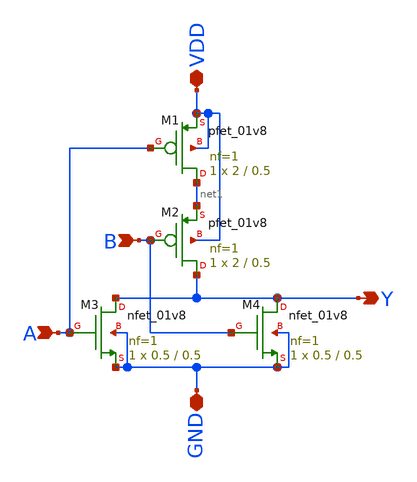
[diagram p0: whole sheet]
** sch_path: FinalProj/NOR.sch
**.subckt NOR B A GND VDD Y
*.ipin B
*.ipin A
*.iopin GND
*.iopin VDD
*.opin Y
XM1 net1 A VDD VDD sky130_fd_pr__pfet_01v8 L=0.5 W=2 nf=1 ad='int((nf+1)/2) * W/nf * 0.29' as='int((nf+2)/2) * W/nf * 0.29'
+ pd='2*int((nf+1)/2) * (W/nf + 0.29)' ps='2*int((nf+2)/2) * (W/nf + 0.29)' nrd='0.29 / W' nrs='0.29 / W'
+ sa=0 sb=0 sd=0 mult=1 m=1
XM2 Y B net1 VDD sky130_fd_pr__pfet_01v8 L=0.5 W=2 nf=1 ad='int((nf+1)/2) * W/nf * 0.29' as='int((nf+2)/2) * W/nf * 0.29'
+ pd='2*int((nf+1)/2) * (W/nf + 0.29)' ps='2*int((nf+2)/2) * (W/nf + 0.29)' nrd='0.29 / W' nrs='0.29 / W'
+ sa=0 sb=0 sd=0 mult=1 m=1
XM3 Y A GND GND sky130_fd_pr__nfet_01v8 L=0.5 W=0.5 nf=1 ad='int((nf+1)/2) * W/nf * 0.29' as='int((nf+2)/2) * W/nf * 0.29'
+ pd='2*int((nf+1)/2) * (W/nf + 0.29)' ps='2*int((nf+2)/2) * (W/nf + 0.29)' nrd='0.29 / W' nrs='0.29 / W'
+ sa=0 sb=0 sd=0 mult=1 m=1
XM4 Y B GND GND sky130_fd_pr__nfet_01v8 L=0.5 W=0.5 nf=1 ad='int((nf+1)/2) * W/nf * 0.29' as='int((nf+2)/2) * W/nf * 0.29'
+ pd='2*int((nf+1)/2) * (W/nf + 0.29)' ps='2*int((nf+2)/2) * (W/nf + 0.29)' nrd='0.29 / W' nrs='0.29 / W'
+ sa=0 sb=0 sd=0 mult=1 m=1
**.ends
.end
